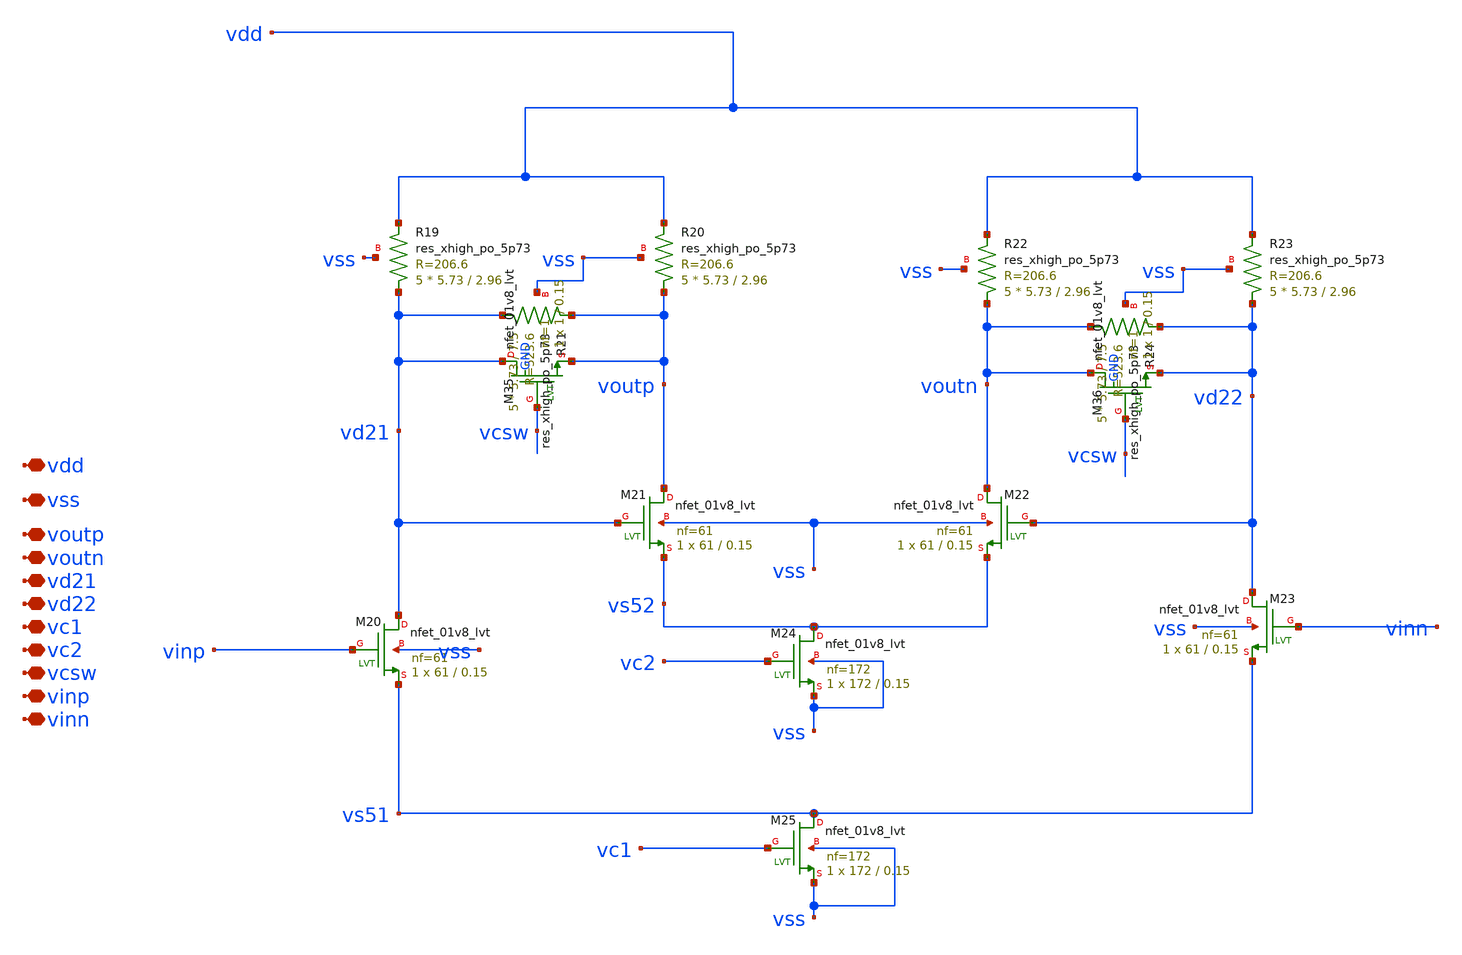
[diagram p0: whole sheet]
** sch_path: design/vga/norm_stages.sch
**.subckt norm_stages vdd vss voutp voutn vd21 vd22 vc1 vc2 vcsw vinp vinn
*.iopin vdd
*.iopin vss
*.iopin voutp
*.iopin voutn
*.iopin vd21
*.iopin vd22
*.iopin vc1
*.iopin vc2
*.iopin vcsw
*.iopin vinp
*.iopin vinn
XR19 vd21 vdd vss sky130_fd_pr__res_xhigh_po_5p73 L=2.96 mult=5 m=5
XR20 voutp vdd vss sky130_fd_pr__res_xhigh_po_5p73 L=2.96 mult=5 m=5
XR21 vd21 voutp vss sky130_fd_pr__res_xhigh_po_5p73 L=7.5 mult=5 m=5
XR22 voutn vdd vss sky130_fd_pr__res_xhigh_po_5p73 L=2.96 mult=5 m=5
XR23 vd22 vdd vss sky130_fd_pr__res_xhigh_po_5p73 L=2.96 mult=5 m=5
XR24 voutn vd22 vss sky130_fd_pr__res_xhigh_po_5p73 L=7.5 mult=5 m=5
XM20 vd21 vinp vs51 vss sky130_fd_pr__nfet_01v8_lvt L=0.15 W=61 nf=61 ad='int((nf+1)/2) * W/nf * 0.29'
+ as='int((nf+2)/2) * W/nf * 0.29' pd='2*int((nf+1)/2) * (W/nf + 0.29)' ps='2*int((nf+2)/2) * (W/nf + 0.29)'
+ nrd='0.29 / W' nrs='0.29 / W' sa=0 sb=0 sd=0 mult=1 m=1
XM21 voutp vd21 vs52 vss sky130_fd_pr__nfet_01v8_lvt L=0.15 W=61 nf=61 ad='int((nf+1)/2) * W/nf * 0.29'
+ as='int((nf+2)/2) * W/nf * 0.29' pd='2*int((nf+1)/2) * (W/nf + 0.29)' ps='2*int((nf+2)/2) * (W/nf + 0.29)'
+ nrd='0.29 / W' nrs='0.29 / W' sa=0 sb=0 sd=0 mult=1 m=1
XM22 voutn vd22 vs52 vss sky130_fd_pr__nfet_01v8_lvt L=0.15 W=61 nf=61 ad='int((nf+1)/2) * W/nf * 0.29'
+ as='int((nf+2)/2) * W/nf * 0.29' pd='2*int((nf+1)/2) * (W/nf + 0.29)' ps='2*int((nf+2)/2) * (W/nf + 0.29)'
+ nrd='0.29 / W' nrs='0.29 / W' sa=0 sb=0 sd=0 mult=1 m=1
XM23 vd22 vinn vs51 vss sky130_fd_pr__nfet_01v8_lvt L=0.15 W=61 nf=61 ad='int((nf+1)/2) * W/nf * 0.29'
+ as='int((nf+2)/2) * W/nf * 0.29' pd='2*int((nf+1)/2) * (W/nf + 0.29)' ps='2*int((nf+2)/2) * (W/nf + 0.29)'
+ nrd='0.29 / W' nrs='0.29 / W' sa=0 sb=0 sd=0 mult=1 m=1
XM24 vs52 vc2 vss vss sky130_fd_pr__nfet_01v8_lvt L=0.15 W=172 nf=172 ad='int((nf+1)/2) * W/nf * 0.29'
+ as='int((nf+2)/2) * W/nf * 0.29' pd='2*int((nf+1)/2) * (W/nf + 0.29)' ps='2*int((nf+2)/2) * (W/nf + 0.29)'
+ nrd='0.29 / W' nrs='0.29 / W' sa=0 sb=0 sd=0 mult=1 m=1
XM25 vs51 vc1 vss vss sky130_fd_pr__nfet_01v8_lvt L=0.15 W=172 nf=172 ad='int((nf+1)/2) * W/nf * 0.29'
+ as='int((nf+2)/2) * W/nf * 0.29' pd='2*int((nf+1)/2) * (W/nf + 0.29)' ps='2*int((nf+2)/2) * (W/nf + 0.29)'
+ nrd='0.29 / W' nrs='0.29 / W' sa=0 sb=0 sd=0 mult=1 m=1
XM35 vd21 vcsw voutp GND sky130_fd_pr__nfet_01v8_lvt L=0.15 W=1 nf=1 ad='int((nf+1)/2) * W/nf * 0.29'
+ as='int((nf+2)/2) * W/nf * 0.29' pd='2*int((nf+1)/2) * (W/nf + 0.29)' ps='2*int((nf+2)/2) * (W/nf + 0.29)'
+ nrd='0.29 / W' nrs='0.29 / W' sa=0 sb=0 sd=0 mult=1 m=1
XM36 voutn vcsw vd22 GND sky130_fd_pr__nfet_01v8_lvt L=0.15 W=1 nf=1 ad='int((nf+1)/2) * W/nf * 0.29'
+ as='int((nf+2)/2) * W/nf * 0.29' pd='2*int((nf+1)/2) * (W/nf + 0.29)' ps='2*int((nf+2)/2) * (W/nf + 0.29)'
+ nrd='0.29 / W' nrs='0.29 / W' sa=0 sb=0 sd=0 mult=1 m=1
**.ends
.end
